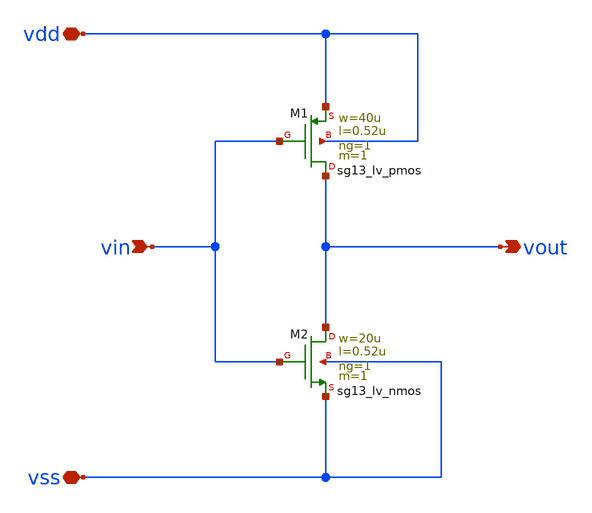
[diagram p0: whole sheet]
** sch_path: Designs/Analog_Inverter/Schematics/Analog_Inverter/Analog_Inverter.sch
* (c) 2024 Hrishikesh, @HSB
**.subckt Analog_Inverter vin vdd vss vout
*.ipin vin
*.iopin vdd
*.iopin vss
*.opin vout
XM1 vout vin vdd vdd sg13_lv_pmos w=40u l=0.52u ng=1 m=1 mm_ok=1
XM2 vout vin vss vss sg13_lv_nmos w=20u l=0.52u ng=1 m=1 mm_ok=1
**.ends
.end
